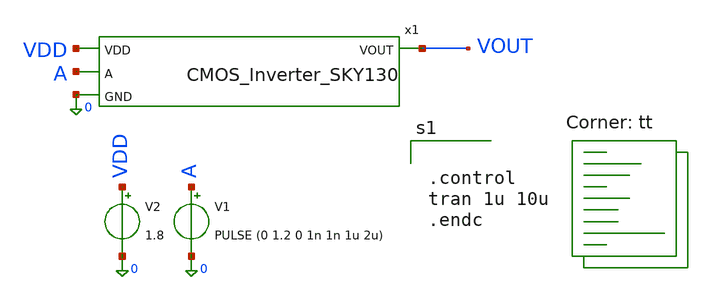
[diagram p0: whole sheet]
** sch_path: CMOS_Inverter_SKY130_testbench.sch
**.subckt CMOS_Inverter_SKY130_testbench
x1 VDD A VOUT 0 CMOS_Inverter_SKY130
V1 A 0 PULSE (0 1.2 0 1n 1n 1u 2u)
V2 VDD 0 1.8
**** begin user architecture code
.lib $::SKYWATER_MODELS/sky130.lib.spice tt


.control
tran 1u 10u
.endc


**** end user architecture code
**.ends

* expanding   symbol:  CMOS_Inverter_SKY130.sym # of pins=4
** sym_path: CMOS_Inverter_SKY130.sym
** sch_path: CMOS_Inverter_SKY130.sch
.subckt CMOS_Inverter_SKY130 VDD A VOUT GND
*.ipin A
*.ipin VDD
*.ipin GND
*.opin VOUT
XM18 VOUT A GND GND sky130_fd_pr__nfet_01v8 L=0.15 W=7 nf=1 ad='int((nf+1)/2) * W/nf * 0.29' as='int((nf+2)/2) * W/nf * 0.29'
+ pd='2*int((nf+1)/2) * (W/nf + 0.29)' ps='2*int((nf+2)/2) * (W/nf + 0.29)' nrd='0.29 / W' nrs='0.29 / W'
+ sa=0 sb=0 sd=0 mult=1 m=1
XT1 VOUT A VDD VDD sky130_fd_pr__pfet_01v8 L=0.15 W=21 nf=1 ad='int((1 + 1)/2) * 21 / 1 * 0.29' as='int((1 + 2)/2) * 21 / 1 * 0.29'
+ pd='2*int((1 + 1)/2) * (21 / 1 + 0.29)' ps='2*int((1 + 2)/2) * (21 / 1 + 0.29)' nrd='0.29 / 21 ' nrs='0.29 / 21 '
+ sa=0 sb=0 sd=0 mult=1 m=1
.ends

.end
